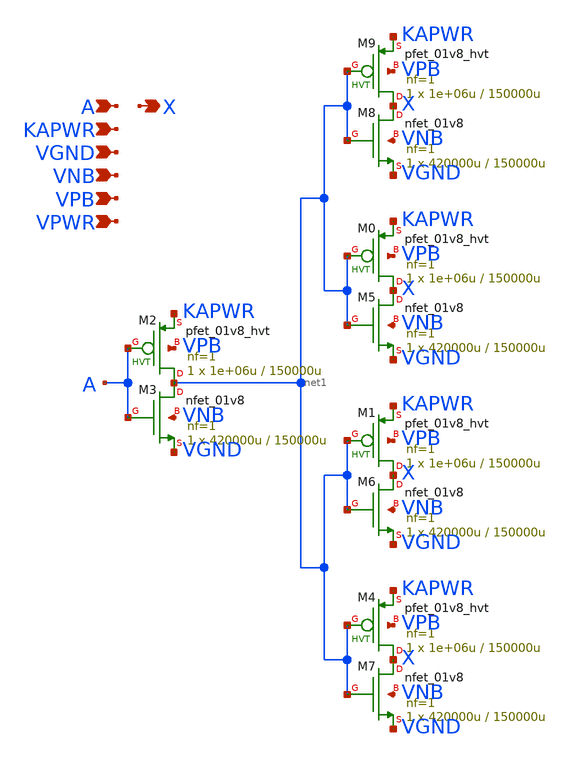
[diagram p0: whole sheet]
** sch_path: schematics/lpflow_clkbufkapwr/sky130_fd_sc_hd__lpflow_clkbufkapwr_4.sch
**.subckt sky130_fd_sc_hd__lpflow_clkbufkapwr_4 A KAPWR VGND VNB VPB VPWR X
*.ipin A
*.ipin KAPWR
*.ipin VGND
*.ipin VNB
*.ipin VPB
*.ipin VPWR
*.opin X
XM2 net1 A KAPWR VPB sky130_fd_pr__pfet_01v8_hvt L=150000u W=1e+06u nf=1 ad='int((1 + 1)/2) * 1e+06u / 1 * 0.29'
+ as='int((1 + 2)/2) * 1e+06u / 1 * 0.29' pd='2*int((1 + 1)/2) * (1e+06u / 1 + 0.29)' ps='2*int((1 + 2)/2) * (1e+06u / 1 + 0.29)'
+ nrd='0.29 / 1e+06u ' nrs='0.29 / 1e+06u ' sa=0 sb=0 sd=0 mult=1 m=1
XM0 X net1 KAPWR VPB sky130_fd_pr__pfet_01v8_hvt L=150000u W=1e+06u nf=1 ad='int((1 + 1)/2) * 1e+06u / 1 * 0.29'
+ as='int((1 + 2)/2) * 1e+06u / 1 * 0.29' pd='2*int((1 + 1)/2) * (1e+06u / 1 + 0.29)' ps='2*int((1 + 2)/2) * (1e+06u / 1 + 0.29)'
+ nrd='0.29 / 1e+06u ' nrs='0.29 / 1e+06u ' sa=0 sb=0 sd=0 mult=1 m=1
XM1 X net1 KAPWR VPB sky130_fd_pr__pfet_01v8_hvt L=150000u W=1e+06u nf=1 ad='int((1 + 1)/2) * 1e+06u / 1 * 0.29'
+ as='int((1 + 2)/2) * 1e+06u / 1 * 0.29' pd='2*int((1 + 1)/2) * (1e+06u / 1 + 0.29)' ps='2*int((1 + 2)/2) * (1e+06u / 1 + 0.29)'
+ nrd='0.29 / 1e+06u ' nrs='0.29 / 1e+06u ' sa=0 sb=0 sd=0 mult=1 m=1
XM4 X net1 KAPWR VPB sky130_fd_pr__pfet_01v8_hvt L=150000u W=1e+06u nf=1 ad='int((1 + 1)/2) * 1e+06u / 1 * 0.29'
+ as='int((1 + 2)/2) * 1e+06u / 1 * 0.29' pd='2*int((1 + 1)/2) * (1e+06u / 1 + 0.29)' ps='2*int((1 + 2)/2) * (1e+06u / 1 + 0.29)'
+ nrd='0.29 / 1e+06u ' nrs='0.29 / 1e+06u ' sa=0 sb=0 sd=0 mult=1 m=1
XM9 X net1 KAPWR VPB sky130_fd_pr__pfet_01v8_hvt L=150000u W=1e+06u nf=1 ad='int((1 + 1)/2) * 1e+06u / 1 * 0.29'
+ as='int((1 + 2)/2) * 1e+06u / 1 * 0.29' pd='2*int((1 + 1)/2) * (1e+06u / 1 + 0.29)' ps='2*int((1 + 2)/2) * (1e+06u / 1 + 0.29)'
+ nrd='0.29 / 1e+06u ' nrs='0.29 / 1e+06u ' sa=0 sb=0 sd=0 mult=1 m=1
XM3 net1 A VGND VNB sky130_fd_pr__nfet_01v8 L=150000u W=420000u nf=1 ad='int((1 + 1)/2) * 420000u / 1 * 0.29'
+ as='int((1 + 2)/2) * 420000u / 1 * 0.29' pd='2*int((1 + 1)/2) * (420000u / 1 + 0.29)' ps='2*int((1 + 2)/2) * (420000u / 1 + 0.29)'
+ nrd='0.29 / 420000u ' nrs='0.29 / 420000u ' sa=0 sb=0 sd=0 mult=1 m=1
XM5 X net1 VGND VNB sky130_fd_pr__nfet_01v8 L=150000u W=420000u nf=1 ad='int((1 + 1)/2) * 420000u / 1 * 0.29'
+ as='int((1 + 2)/2) * 420000u / 1 * 0.29' pd='2*int((1 + 1)/2) * (420000u / 1 + 0.29)' ps='2*int((1 + 2)/2) * (420000u / 1 + 0.29)'
+ nrd='0.29 / 420000u ' nrs='0.29 / 420000u ' sa=0 sb=0 sd=0 mult=1 m=1
XM6 X net1 VGND VNB sky130_fd_pr__nfet_01v8 L=150000u W=420000u nf=1 ad='int((1 + 1)/2) * 420000u / 1 * 0.29'
+ as='int((1 + 2)/2) * 420000u / 1 * 0.29' pd='2*int((1 + 1)/2) * (420000u / 1 + 0.29)' ps='2*int((1 + 2)/2) * (420000u / 1 + 0.29)'
+ nrd='0.29 / 420000u ' nrs='0.29 / 420000u ' sa=0 sb=0 sd=0 mult=1 m=1
XM7 X net1 VGND VNB sky130_fd_pr__nfet_01v8 L=150000u W=420000u nf=1 ad='int((1 + 1)/2) * 420000u / 1 * 0.29'
+ as='int((1 + 2)/2) * 420000u / 1 * 0.29' pd='2*int((1 + 1)/2) * (420000u / 1 + 0.29)' ps='2*int((1 + 2)/2) * (420000u / 1 + 0.29)'
+ nrd='0.29 / 420000u ' nrs='0.29 / 420000u ' sa=0 sb=0 sd=0 mult=1 m=1
XM8 X net1 VGND VNB sky130_fd_pr__nfet_01v8 L=150000u W=420000u nf=1 ad='int((1 + 1)/2) * 420000u / 1 * 0.29'
+ as='int((1 + 2)/2) * 420000u / 1 * 0.29' pd='2*int((1 + 1)/2) * (420000u / 1 + 0.29)' ps='2*int((1 + 2)/2) * (420000u / 1 + 0.29)'
+ nrd='0.29 / 420000u ' nrs='0.29 / 420000u ' sa=0 sb=0 sd=0 mult=1 m=1
**.ends
.end
